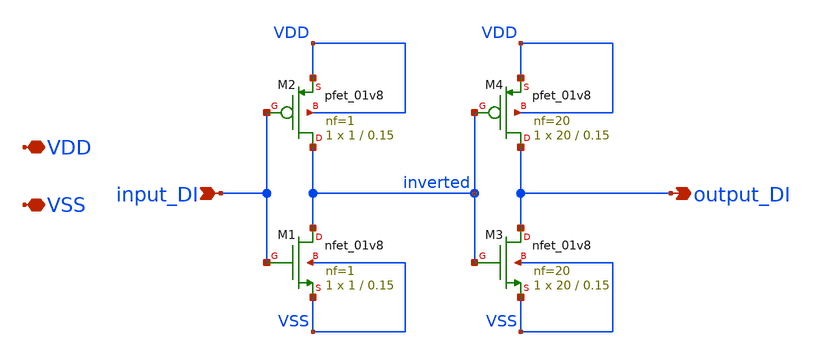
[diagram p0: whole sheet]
** sch_path: xschem/double_inverter.sch
**.subckt double_inverter VDD VSS input_DI output_DI
*.iopin VDD
*.iopin VSS
*.ipin input_DI
*.opin output_DI
XM1 inverted input_DI VSS VSS sky130_fd_pr__nfet_01v8 L=0.15 W=1 nf=1 ad='int((1 + 1)/2) * 1 / 1 * 0.29'
+ as='int((1 + 2)/2) * 1 / 1 * 0.29' pd='2*int((1 + 1)/2) * (1 / 1 + 0.29)' ps='2*int((1 + 2)/2) * (1 / 1 + 0.29)'
+ nrd='0.29 / 1 ' nrs='0.29 / 1 ' sa=0 sb=0 sd=0 mult=1 m=1
XM2 inverted input_DI VDD VDD sky130_fd_pr__pfet_01v8 L=0.15 W=1 nf=1 ad='int((1 + 1)/2) * 1 / 1 * 0.29'
+ as='int((1 + 2)/2) * 1 / 1 * 0.29' pd='2*int((1 + 1)/2) * (1 / 1 + 0.29)' ps='2*int((1 + 2)/2) * (1 / 1 + 0.29)'
+ nrd='0.29 / 1 ' nrs='0.29 / 1 ' sa=0 sb=0 sd=0 mult=1 m=1
XM3 output_DI inverted VSS VSS sky130_fd_pr__nfet_01v8 L=0.15 W=20 nf=20 ad='int((20 + 1)/2) * 20 / 20 * 0.29'
+ as='int((20 + 2)/2) * 20 / 20 * 0.29' pd='2*int((20 + 1)/2) * (20 / 20 + 0.29)' ps='2*int((20 + 2)/2) * (20 / 20 + 0.29)'
+ nrd='0.29 / 20 ' nrs='0.29 / 20 ' sa=0 sb=0 sd=0 mult=1 m=1
XM4 output_DI inverted VDD VDD sky130_fd_pr__pfet_01v8 L=0.15 W=20 nf=20 ad='int((20 + 1)/2) * 20 / 20 * 0.29'
+ as='int((20 + 2)/2) * 20 / 20 * 0.29' pd='2*int((20 + 1)/2) * (20 / 20 + 0.29)' ps='2*int((20 + 2)/2) * (20 / 20 + 0.29)'
+ nrd='0.29 / 20 ' nrs='0.29 / 20 ' sa=0 sb=0 sd=0 mult=1 m=1
**.ends
.end
